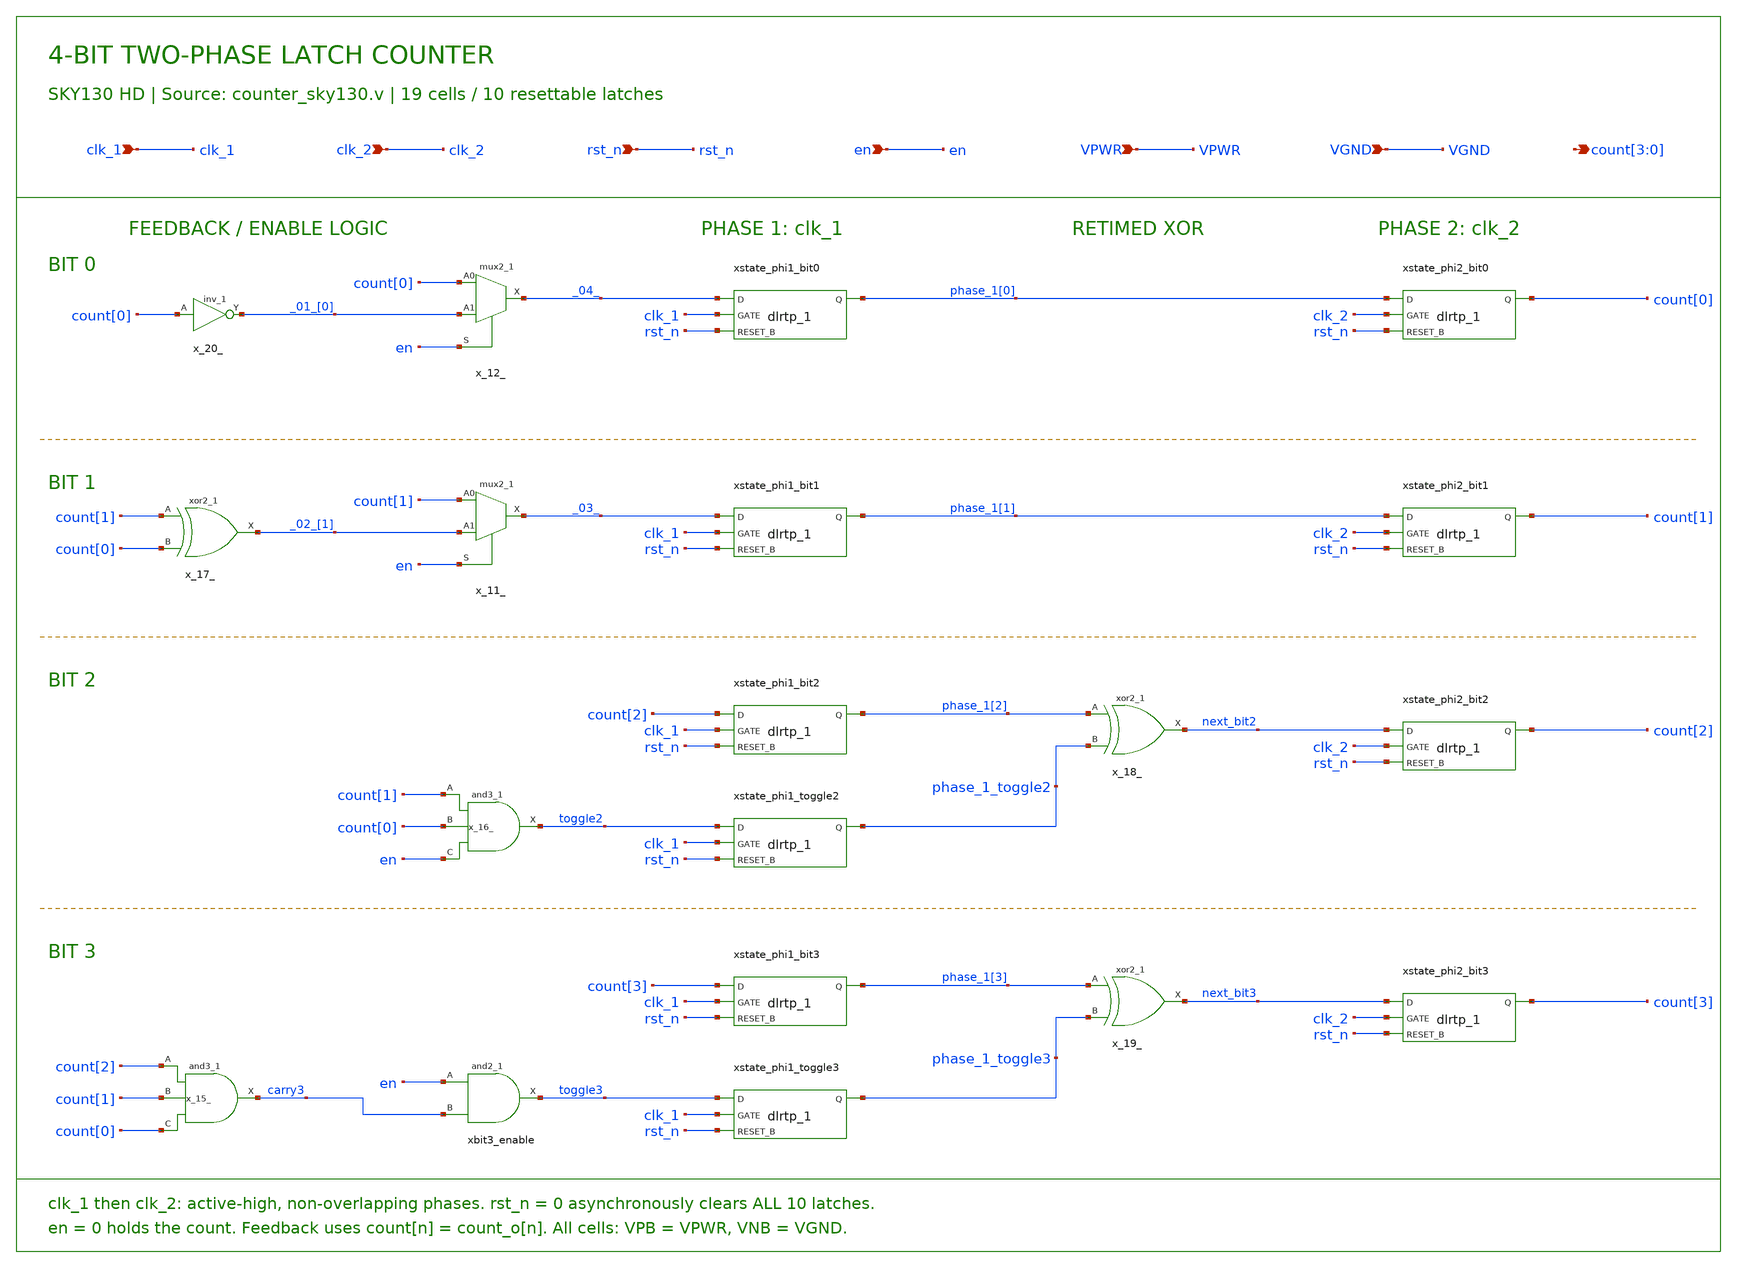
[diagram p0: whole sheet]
** sch_path: examples/counter/counter_latch_mux_1/counter_sky130.sch
**.subckt counter_sky130 clk_1 clk_2 rst_n en VPWR VGND count[3],count[2],count[1],count[0]
*.ipin clk_1
*.ipin clk_2
*.ipin rst_n
*.ipin en
*.ipin VPWR
*.ipin VGND
*.opin count[3],count[2],count[1],count[0]
xstate_phi1_bit0 _04_ clk_1 rst_n VGND VGND VPWR VPWR phase_1[0] sky130_fd_sc_hd__dlrtp_1
x_12_ count[0] _01_[0] en VGND VGND VPWR VPWR _04_ sky130_fd_sc_hd__mux2_1
x_20_ count[0] VGND VGND VPWR VPWR _01_[0] sky130_fd_sc_hd__inv_1
xstate_phi2_bit0 phase_1[0] clk_2 rst_n VGND VGND VPWR VPWR count[0] sky130_fd_sc_hd__dlrtp_1
xstate_phi1_bit1 _03_ clk_1 rst_n VGND VGND VPWR VPWR phase_1[1] sky130_fd_sc_hd__dlrtp_1
x_11_ count[1] _02_[1] en VGND VGND VPWR VPWR _03_ sky130_fd_sc_hd__mux2_1
x_17_ count[1] count[0] VGND VGND VPWR VPWR _02_[1] sky130_fd_sc_hd__xor2_1
xstate_phi2_bit1 phase_1[1] clk_2 rst_n VGND VGND VPWR VPWR count[1] sky130_fd_sc_hd__dlrtp_1
xstate_phi1_bit2 count[2] clk_1 rst_n VGND VGND VPWR VPWR phase_1[2] sky130_fd_sc_hd__dlrtp_1
x_18_ phase_1[2] phase_1_toggle2 VGND VGND VPWR VPWR next_bit2 sky130_fd_sc_hd__xor2_1
xstate_phi2_bit2 next_bit2 clk_2 rst_n VGND VGND VPWR VPWR count[2] sky130_fd_sc_hd__dlrtp_1
xstate_phi1_toggle2 toggle2 clk_1 rst_n VGND VGND VPWR VPWR phase_1_toggle2 sky130_fd_sc_hd__dlrtp_1
x_16_ count[1] count[0] en VGND VGND VPWR VPWR toggle2 sky130_fd_sc_hd__and3_1
xstate_phi1_bit3 count[3] clk_1 rst_n VGND VGND VPWR VPWR phase_1[3] sky130_fd_sc_hd__dlrtp_1
x_19_ phase_1[3] phase_1_toggle3 VGND VGND VPWR VPWR next_bit3 sky130_fd_sc_hd__xor2_1
xstate_phi2_bit3 next_bit3 clk_2 rst_n VGND VGND VPWR VPWR count[3] sky130_fd_sc_hd__dlrtp_1
xstate_phi1_toggle3 toggle3 clk_1 rst_n VGND VGND VPWR VPWR phase_1_toggle3 sky130_fd_sc_hd__dlrtp_1
x_15_ count[2] count[1] count[0] VGND VGND VPWR VPWR carry3 sky130_fd_sc_hd__and3_1
xbit3_enable en carry3 VGND VGND VPWR VPWR toggle3 sky130_fd_sc_hd__and2_1
**.ends
.end
